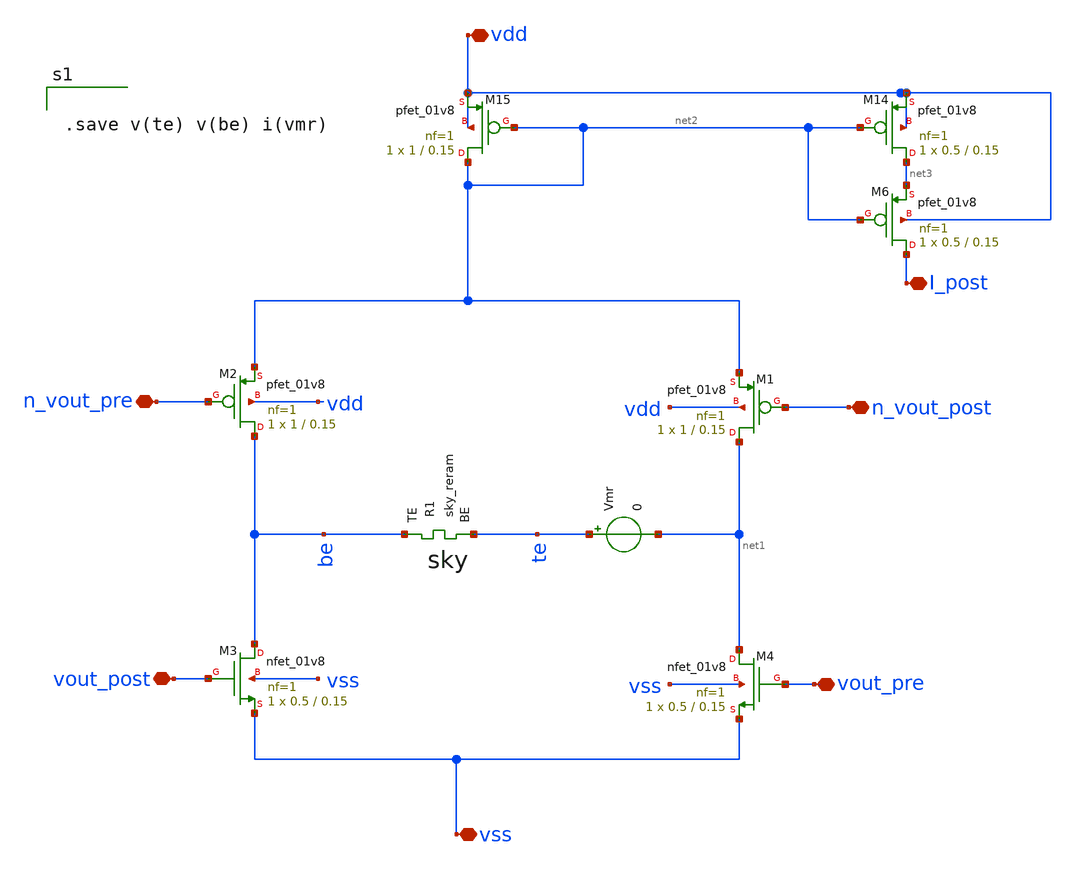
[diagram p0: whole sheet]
** sch_path: Synapse/stdp_min_sky.sch
**.subckt stdp_min_sky vdd vss vout_post vout_pre I_post n_vout_post n_vout_pre
*.iopin vdd
*.iopin vss
*.iopin vout_post
*.iopin vout_pre
*.iopin I_post
*.iopin n_vout_post
*.iopin n_vout_pre
XM3 be vout_post vss vss sky130_fd_pr__nfet_01v8 L=0.15 W=0.5 nf=1 ad='int((nf+1)/2) * W/nf * 0.29' as='int((nf+2)/2) * W/nf * 0.29'
+ pd='2*int((nf+1)/2) * (W/nf + 0.29)' ps='2*int((nf+2)/2) * (W/nf + 0.29)' nrd='0.29 / W' nrs='0.29 / W'
+ sa=0 sb=0 sd=0 mult=1 m=1
XM4 net1 vout_pre vss vss sky130_fd_pr__nfet_01v8 L=0.15 W=0.5 nf=1 ad='int((nf+1)/2) * W/nf * 0.29'
+ as='int((nf+2)/2) * W/nf * 0.29' pd='2*int((nf+1)/2) * (W/nf + 0.29)' ps='2*int((nf+2)/2) * (W/nf + 0.29)'
+ nrd='0.29 / W' nrs='0.29 / W' sa=0 sb=0 sd=0 mult=1 m=1
XM14 net3 net2 vdd vdd sky130_fd_pr__pfet_01v8 L=0.15 W=0.5 nf=1 ad='int((nf+1)/2) * W/nf * 0.29' as='int((nf+2)/2) * W/nf * 0.29'
+ pd='2*int((nf+1)/2) * (W/nf + 0.29)' ps='2*int((nf+2)/2) * (W/nf + 0.29)' nrd='0.29 / W' nrs='0.29 / W'
+ sa=0 sb=0 sd=0 mult=1 m=1
XM15 net2 net2 vdd vdd sky130_fd_pr__pfet_01v8 L=0.15 W=1 nf=1 ad='int((nf+1)/2) * W/nf * 0.29' as='int((nf+2)/2) * W/nf * 0.29'
+ pd='2*int((nf+1)/2) * (W/nf + 0.29)' ps='2*int((nf+2)/2) * (W/nf + 0.29)' nrd='0.29 / W' nrs='0.29 / W'
+ sa=0 sb=0 sd=0 mult=1 m=1
Vmr te net1 0
.save i(vmr)
XM1 net1 n_vout_post net2 vdd sky130_fd_pr__pfet_01v8 L=0.15 W=1 nf=1 ad='int((nf+1)/2) * W/nf * 0.29'
+ as='int((nf+2)/2) * W/nf * 0.29' pd='2*int((nf+1)/2) * (W/nf + 0.29)' ps='2*int((nf+2)/2) * (W/nf + 0.29)'
+ nrd='0.29 / W' nrs='0.29 / W' sa=0 sb=0 sd=0 mult=1 m=1
XM2 be n_vout_pre net2 vdd sky130_fd_pr__pfet_01v8 L=0.15 W=1 nf=1 ad='int((nf+1)/2) * W/nf * 0.29' as='int((nf+2)/2) * W/nf * 0.29'
+ pd='2*int((nf+1)/2) * (W/nf + 0.29)' ps='2*int((nf+2)/2) * (W/nf + 0.29)' nrd='0.29 / W' nrs='0.29 / W'
+ sa=0 sb=0 sd=0 mult=1 m=1
XM6 I_post net2 net3 vdd sky130_fd_pr__pfet_01v8 L=0.15 W=0.5 nf=1 ad='int((nf+1)/2) * W/nf * 0.29' as='int((nf+2)/2) * W/nf * 0.29'
+ pd='2*int((nf+1)/2) * (W/nf + 0.29)' ps='2*int((nf+2)/2) * (W/nf + 0.29)' nrd='0.29 / W' nrs='0.29 / W'
+ sa=0 sb=0 sd=0 mult=1 m=1
XR1 be te sky_reram
**** begin user architecture code


.save v(te) v(be) i(vmr)


**** end user architecture code
**.ends
.end
